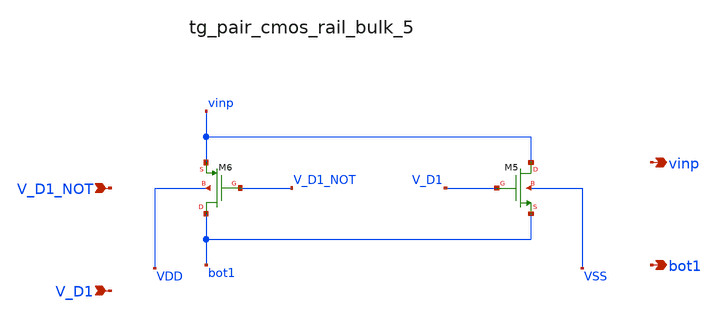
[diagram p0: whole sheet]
** sch_path: analog-db/raw/sw_003_binary_capbank/hier/blocks/tg_pair_cmos_rail_bulk_5.sch
**.subckt tg_pair_cmos_rail_bulk_5 V_D1_NOT V_D1 vinp bot1
*.ipin V_D1_NOT
*.ipin V_D1
*.opin vinp
*.opin bot1
XM5 vinp V_D1 bot1 VSS sg13_lv_nmos w=x_dut_xm5_w l=x_dut_xm5_l ng=1 m=x_dut_xm5_m
XM6 bot1 V_D1_NOT vinp VDD sg13_lv_pmos w=x_dut_xm6_w l=x_dut_xm6_l ng=1 m=x_dut_xm6_m
**.ends
.end
